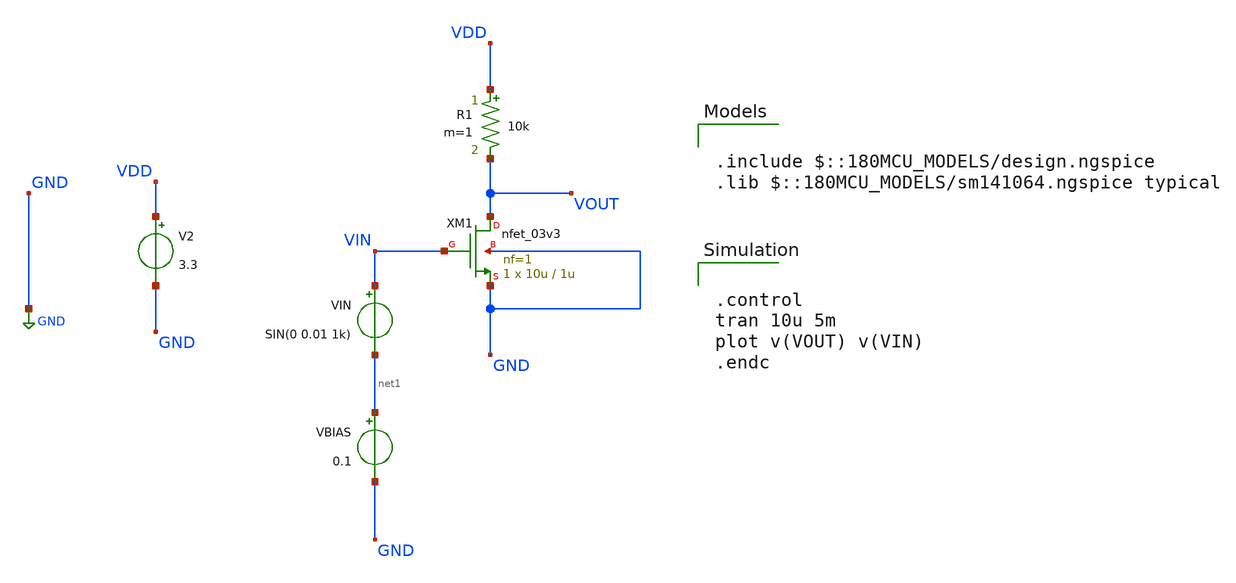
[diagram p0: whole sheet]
** sch_path: designs/sophiazhu/session_1/cs_res_load_poor_bias.sch
**.subckt cs_res_load_poor_bias
XM1 VOUT VIN GND GND nfet_03v3 L=1u W=10u nf=1 ad='int((nf+1)/2) * W/nf * 0.18u' as='int((nf+2)/2) * W/nf * 0.18u'
+ pd='2*int((nf+1)/2) * (W/nf + 0.18u)' ps='2*int((nf+2)/2) * (W/nf + 0.18u)' nrd='0.18u / W' nrs='0.18u / W'
+ sa=0 sb=0 sd=0 m=1
R1 VDD VOUT 10k m=1
V2 VDD GND 3.3
VBIAS net1 GND 0.1
VIN VIN net1 SIN(0 0.01 1k)
**** begin user architecture code


.control
tran 10u 5m
plot v(VOUT) v(VIN)
.endc



.include $::180MCU_MODELS/design.ngspice
.lib $::180MCU_MODELS/sm141064.ngspice typical

**** end user architecture code
**.ends
.GLOBAL GND
.end
